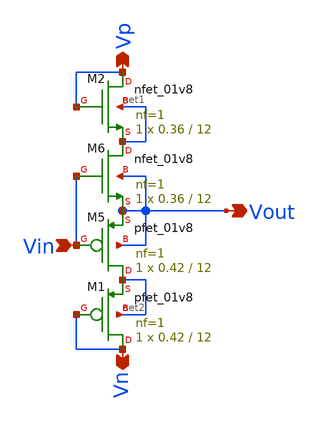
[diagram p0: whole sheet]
** sch_path: xschem/Vth_sch/Symbol/th01_test.sch
**.subckt th01_test Vn Vp Vin Vout
*.opin Vn
*.opin Vp
*.ipin Vin
*.opin Vout
XM1 Vn Vn net2 net2 sky130_fd_pr__pfet_01v8 L=12 W=0.42 nf=1 ad='int((nf+1)/2) * W/nf * 0.29' as='int((nf+2)/2) * W/nf * 0.29'
+ pd='2*int((nf+1)/2) * (W/nf + 0.29)' ps='2*int((nf+2)/2) * (W/nf + 0.29)' nrd='0.29 / W' nrs='0.29 / W'
+ sa=0 sb=0 sd=0 mult=1 m=1
XM2 Vp Vp net1 net1 sky130_fd_pr__nfet_01v8 L=12 W=0.36 nf=1 ad='int((nf+1)/2) * W/nf * 0.29' as='int((nf+2)/2) * W/nf * 0.29'
+ pd='2*int((nf+1)/2) * (W/nf + 0.29)' ps='2*int((nf+2)/2) * (W/nf + 0.29)' nrd='0.29 / W' nrs='0.29 / W'
+ sa=0 sb=0 sd=0 mult=1 m=1
XM5 net2 Vin Vout Vout sky130_fd_pr__pfet_01v8 L=12 W=0.42 nf=1 ad='int((nf+1)/2) * W/nf * 0.29' as='int((nf+2)/2) * W/nf * 0.29'
+ pd='2*int((nf+1)/2) * (W/nf + 0.29)' ps='2*int((nf+2)/2) * (W/nf + 0.29)' nrd='0.29 / W' nrs='0.29 / W'
+ sa=0 sb=0 sd=0 mult=1 m=1
XM6 net1 Vin Vout Vout sky130_fd_pr__nfet_01v8 L=12 W=0.36 nf=1 ad='int((nf+1)/2) * W/nf * 0.29' as='int((nf+2)/2) * W/nf * 0.29'
+ pd='2*int((nf+1)/2) * (W/nf + 0.29)' ps='2*int((nf+2)/2) * (W/nf + 0.29)' nrd='0.29 / W' nrs='0.29 / W'
+ sa=0 sb=0 sd=0 mult=1 m=1
**.ends
.end
